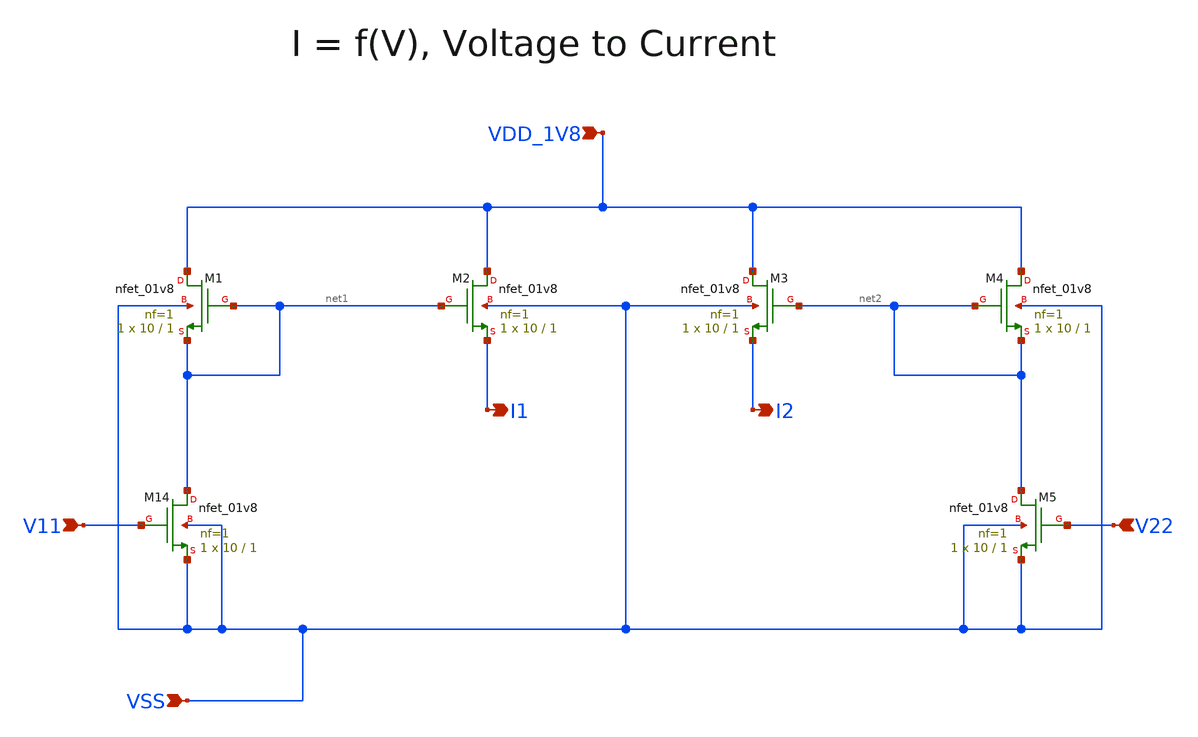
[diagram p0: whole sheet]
** sch_path: design/CNR_GR06_SKY130NM/CNR_GR06_V_to_I.sch
**.subckt CNR_GR06_V_to_I VDD_1V8 VSS I1 I2 V11 V22
*.ipin VDD_1V8
*.ipin VSS
*.opin I1
*.opin I2
*.ipin V11
*.ipin V22
XM14 net1 V11 VSS VSS sky130_fd_pr__nfet_01v8 L=1 W=10 nf=1 ad='int((nf+1)/2) * W/nf * 0.29' as='int((nf+2)/2) * W/nf * 0.29'
+ pd='2*int((nf+1)/2) * (W/nf + 0.29)' ps='2*int((nf+2)/2) * (W/nf + 0.29)' nrd='0.29 / W' nrs='0.29 / W'
+ sa=0 sb=0 sd=0 mult=1 m=1
XM1 VDD_1V8 net1 net1 VSS sky130_fd_pr__nfet_01v8 L=1 W=10 nf=1 ad='int((nf+1)/2) * W/nf * 0.29' as='int((nf+2)/2) * W/nf * 0.29'
+ pd='2*int((nf+1)/2) * (W/nf + 0.29)' ps='2*int((nf+2)/2) * (W/nf + 0.29)' nrd='0.29 / W' nrs='0.29 / W'
+ sa=0 sb=0 sd=0 mult=1 m=1
XM2 VDD_1V8 net1 I1 VSS sky130_fd_pr__nfet_01v8 L=1 W=10 nf=1 ad='int((nf+1)/2) * W/nf * 0.29' as='int((nf+2)/2) * W/nf * 0.29'
+ pd='2*int((nf+1)/2) * (W/nf + 0.29)' ps='2*int((nf+2)/2) * (W/nf + 0.29)' nrd='0.29 / W' nrs='0.29 / W'
+ sa=0 sb=0 sd=0 mult=1 m=1
XM3 VDD_1V8 net2 I2 VSS sky130_fd_pr__nfet_01v8 L=1 W=10 nf=1 ad='int((nf+1)/2) * W/nf * 0.29' as='int((nf+2)/2) * W/nf * 0.29'
+ pd='2*int((nf+1)/2) * (W/nf + 0.29)' ps='2*int((nf+2)/2) * (W/nf + 0.29)' nrd='0.29 / W' nrs='0.29 / W'
+ sa=0 sb=0 sd=0 mult=1 m=1
XM4 VDD_1V8 net2 net2 VSS sky130_fd_pr__nfet_01v8 L=1 W=10 nf=1 ad='int((nf+1)/2) * W/nf * 0.29' as='int((nf+2)/2) * W/nf * 0.29'
+ pd='2*int((nf+1)/2) * (W/nf + 0.29)' ps='2*int((nf+2)/2) * (W/nf + 0.29)' nrd='0.29 / W' nrs='0.29 / W'
+ sa=0 sb=0 sd=0 mult=1 m=1
XM5 net2 V22 VSS VSS sky130_fd_pr__nfet_01v8 L=1 W=10 nf=1 ad='int((nf+1)/2) * W/nf * 0.29' as='int((nf+2)/2) * W/nf * 0.29'
+ pd='2*int((nf+1)/2) * (W/nf + 0.29)' ps='2*int((nf+2)/2) * (W/nf + 0.29)' nrd='0.29 / W' nrs='0.29 / W'
+ sa=0 sb=0 sd=0 mult=1 m=1
**.ends
.end
